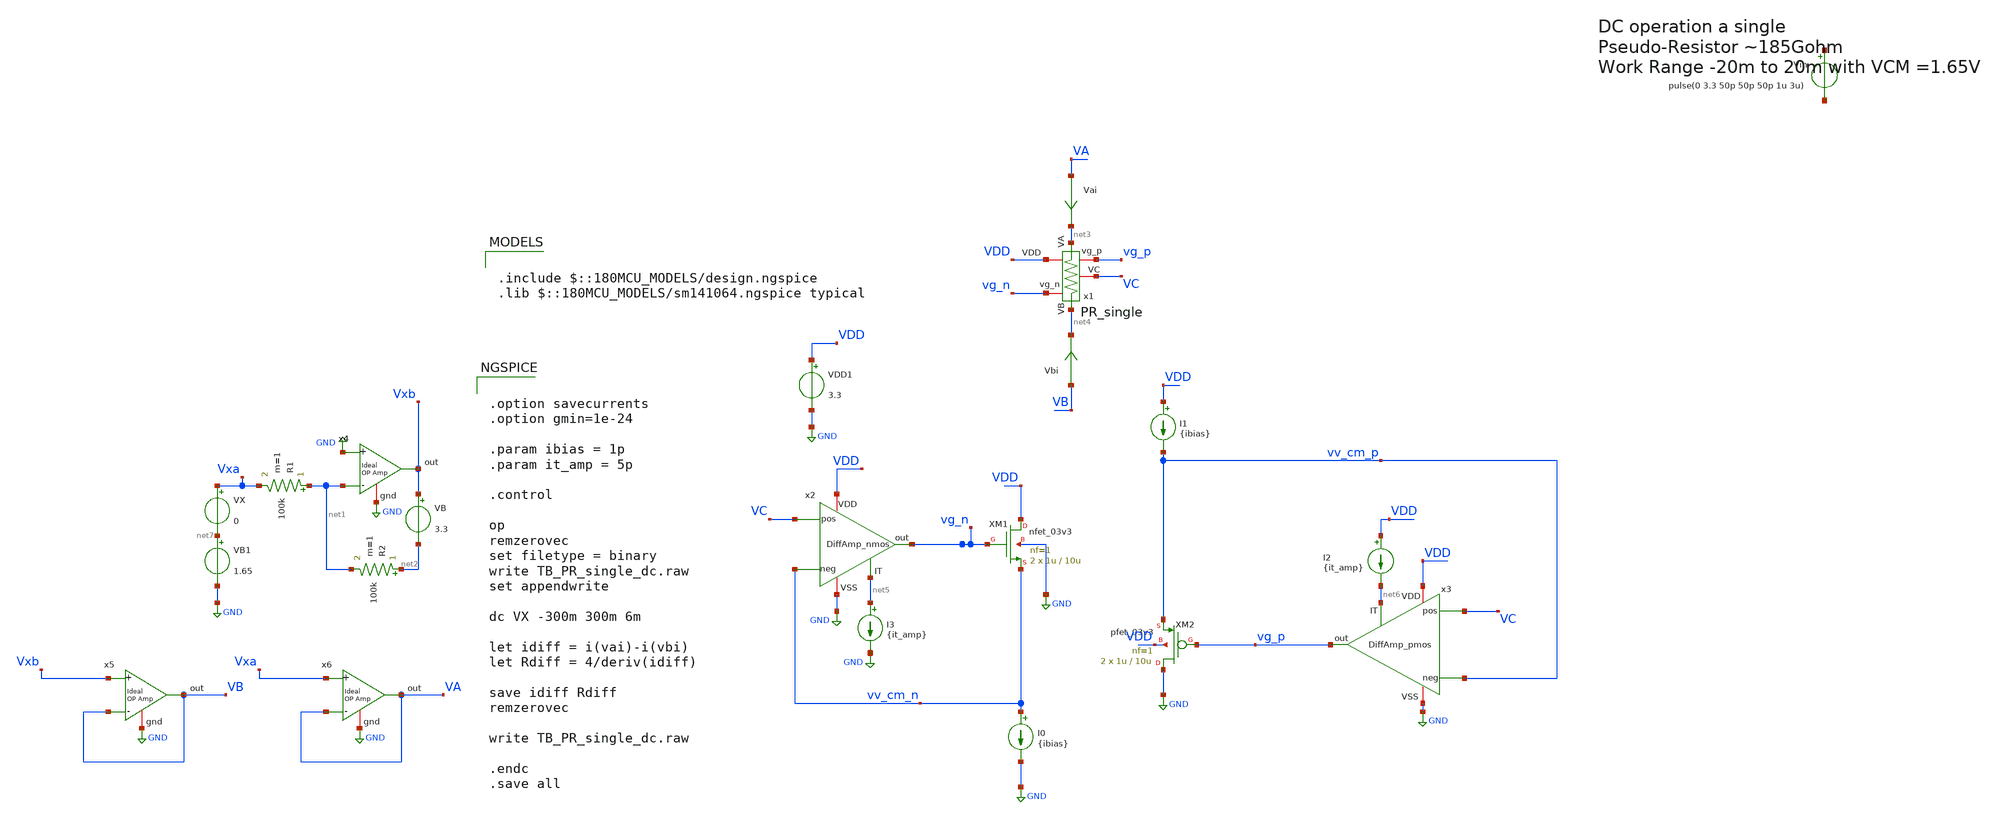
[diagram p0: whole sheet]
** sch_path: TIA/xschem/pseudo_res_dir/TB_PR_single_dc.sch
**.subckt TB_PR_single_dc
x1 VDD net3 vg_p VC vg_n net4 PR_single
XM1 VDD vg_n vv_cm_n GND nfet_03v3 L=10u W=1u nf=1 ad='int((nf+1)/2) * W/nf * 0.18u' as='int((nf+2)/2) * W/nf * 0.18u'
+ pd='2*int((nf+1)/2) * (W/nf + 0.18u)' ps='2*int((nf+2)/2) * (W/nf + 0.18u)' nrd='0.18u / W' nrs='0.18u / W'
+ sa=0 sb=0 sd=0 m=2
XM2 GND vg_p vv_cm_p VDD pfet_03v3 L=10u W=1u nf=1 ad='int((nf+1)/2) * W/nf * 0.18u' as='int((nf+2)/2) * W/nf * 0.18u'
+ pd='2*int((nf+1)/2) * (W/nf + 0.18u)' ps='2*int((nf+2)/2) * (W/nf + 0.18u)' nrd='0.18u / W' nrs='0.18u / W'
+ sa=0 sb=0 sd=0 m=2
I0 vv_cm_n GND {ibias}
I1 VDD vv_cm_p {ibias}
VDD1 VDD GND 3.3
VX Vxa net7 0
VB Vxb net2 3.3
R1 net1 Vxa 100k m=1
R2 net2 net1 100k m=1
VB1 net7 GND 1.65
x4 Vxb GND net1 GND ampOp_ideal
x5 VB Vxb VB GND ampOp_ideal
x6 VA Vxa VA GND ampOp_ideal
Vai VA net3 0
.save i(vai)
Vbi VB net4 0
.save i(vbi)
x2 VDD GND VC vv_cm_n net5 vg_n DiffAmp_nmos
I2 VDD net6 {it_amp}
x3 VDD GND net6 vv_cm_p VC vg_p DiffAmp_pmos
I3 net5 GND {it_amp}
**** begin user architecture code

.include $::180MCU_MODELS/design.ngspice
.lib $::180MCU_MODELS/sm141064.ngspice typical



.option savecurrents
.option gmin=1e-24

.param ibias = 1p
.param it_amp = 5p

.control

op
remzerovec
set filetype = binary
write TB_PR_single_dc.raw
set appendwrite

dc VX -300m 300m 6m

let idiff = i(vai)-i(vbi)
let Rdiff = 4/deriv(idiff)

save idiff Rdiff
remzerovec

write TB_PR_single_dc.raw

.endc
.save all


**** end user architecture code
**.ends
.GLOBAL GND
.end
